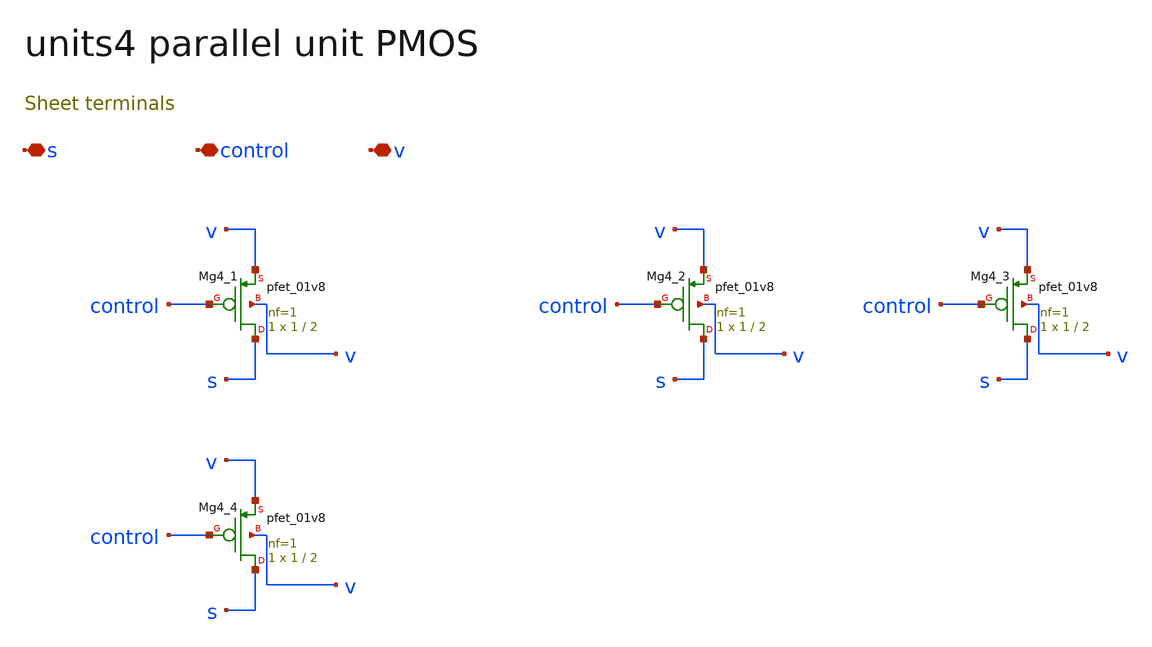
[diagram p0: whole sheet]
** sch_path: review/xschem/units4.sch
**.subckt units4 s control v
*.iopin s
*.iopin control
*.iopin v
XMg4_1 s control v v sky130_fd_pr__pfet_01v8 L=2 W=1 nf=1 ad='int((nf+1)/2) * W/nf * 0.29' as='int((nf+2)/2) * W/nf * 0.29'
+ pd='2*int((nf+1)/2) * (W/nf + 0.29)' ps='2*int((nf+2)/2) * (W/nf + 0.29)' nrd='0.29 / W' nrs='0.29 / W'
+ sa=0 sb=0 sd=0 mult=1 m=1
XMg4_2 s control v v sky130_fd_pr__pfet_01v8 L=2 W=1 nf=1 ad='int((nf+1)/2) * W/nf * 0.29' as='int((nf+2)/2) * W/nf * 0.29'
+ pd='2*int((nf+1)/2) * (W/nf + 0.29)' ps='2*int((nf+2)/2) * (W/nf + 0.29)' nrd='0.29 / W' nrs='0.29 / W'
+ sa=0 sb=0 sd=0 mult=1 m=1
XMg4_3 s control v v sky130_fd_pr__pfet_01v8 L=2 W=1 nf=1 ad='int((nf+1)/2) * W/nf * 0.29' as='int((nf+2)/2) * W/nf * 0.29'
+ pd='2*int((nf+1)/2) * (W/nf + 0.29)' ps='2*int((nf+2)/2) * (W/nf + 0.29)' nrd='0.29 / W' nrs='0.29 / W'
+ sa=0 sb=0 sd=0 mult=1 m=1
XMg4_4 s control v v sky130_fd_pr__pfet_01v8 L=2 W=1 nf=1 ad='int((nf+1)/2) * W/nf * 0.29' as='int((nf+2)/2) * W/nf * 0.29'
+ pd='2*int((nf+1)/2) * (W/nf + 0.29)' ps='2*int((nf+2)/2) * (W/nf + 0.29)' nrd='0.29 / W' nrs='0.29 / W'
+ sa=0 sb=0 sd=0 mult=1 m=1
**.ends
.end
